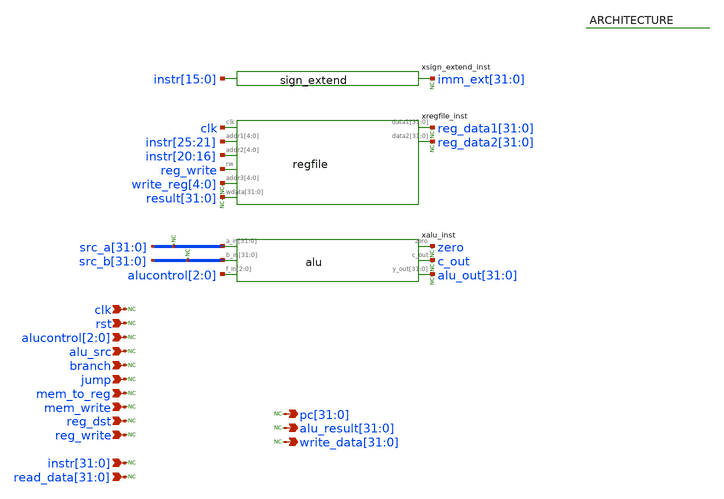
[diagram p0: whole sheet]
** sch_path: sky130A/xschem_libs/mips_cpu/datapath/schematic/datapath.sch
* Licensed under the Apache License, Version 2.0 (the "License");
* you may not use this file except in compliance with the License.
* You may obtain a copy of the License at
* https://www.apache.org/licenses/LICENSE-2.0
* Unless required by applicable law or agreed to in writing, software
* distributed under the License is distributed on an "AS IS" BASIS,
* WITHOUT WARRANTIES OR CONDITIONS OF ANY KIND, either express or implied.
* See the License for the specific language governing permissions and
* limitations under the License.
**.subckt datapath clk rst alucontrol[2],alucontrol[1],alucontrol[0] alu_src branch jump mem_to_reg
*+ reg_dst reg_write
*+ instr[31],instr[30],instr[29],instr[28],instr[27],instr[26],instr[25],instr[24],instr[23],instr[22],instr[21],instr[20],instr[19],instr[18],instr[17],instr[16],instr[15],instr[14],instr[13],instr[12],instr[11],instr[10],instr[9],instr[8],instr[7],instr[6],instr[5],instr[4],instr[3],instr[2],instr[1],instr[0]
*+ pc[31],pc[30],pc[29],pc[28],pc[27],pc[26],pc[25],pc[24],pc[23],pc[22],pc[21],pc[20],pc[19],pc[18],pc[17],pc[16],pc[15],pc[14],pc[13],pc[12],pc[11],pc[10],pc[9],pc[8],pc[7],pc[6],pc[5],pc[4],pc[3],pc[2],pc[1],pc[0]
*+ read_data[31],read_data[30],read_data[29],read_data[28],read_data[27],read_data[26],read_data[25],read_data[24],read_data[23],read_data[22],read_data[21],read_data[20],read_data[19],read_data[18],read_data[17],read_data[16],read_data[15],read_data[14],read_data[13],read_data[12],read_data[11],read_data[10],read_data[9],read_data[8],read_data[7],read_data[6],read_data[5],read_data[4],read_data[3],read_data[2],read_data[1],read_data[0]
*+ alu_result[31],alu_result[30],alu_result[29],alu_result[28],alu_result[27],alu_result[26],alu_result[25],alu_result[24],alu_result[23],alu_result[22],alu_result[21],alu_result[20],alu_result[19],alu_result[18],alu_result[17],alu_result[16],alu_result[15],alu_result[14],alu_result[13],alu_result[12],alu_result[11],alu_result[10],alu_result[9],alu_result[8],alu_result[7],alu_result[6],alu_result[5],alu_result[4],alu_result[3],alu_result[2],alu_result[1],alu_result[0]
*+ write_data[31],write_data[30],write_data[29],write_data[28],write_data[27],write_data[26],write_data[25],write_data[24],write_data[23],write_data[22],write_data[21],write_data[20],write_data[19],write_data[18],write_data[17],write_data[16],write_data[15],write_data[14],write_data[13],write_data[12],write_data[11],write_data[10],write_data[9],write_data[8],write_data[7],write_data[6],write_data[5],write_data[4],write_data[3],write_data[2],write_data[1],write_data[0] mem_write
*.ipin clk
*.ipin rst
*.ipin alucontrol[2],alucontrol[1],alucontrol[0]
*.ipin alu_src
*.ipin branch
*.ipin jump
*.ipin mem_to_reg
*.ipin reg_dst
*.ipin reg_write
*.ipin
*+ instr[31],instr[30],instr[29],instr[28],instr[27],instr[26],instr[25],instr[24],instr[23],instr[22],instr[21],instr[20],instr[19],instr[18],instr[17],instr[16],instr[15],instr[14],instr[13],instr[12],instr[11],instr[10],instr[9],instr[8],instr[7],instr[6],instr[5],instr[4],instr[3],instr[2],instr[1],instr[0]
*.opin
*+ pc[31],pc[30],pc[29],pc[28],pc[27],pc[26],pc[25],pc[24],pc[23],pc[22],pc[21],pc[20],pc[19],pc[18],pc[17],pc[16],pc[15],pc[14],pc[13],pc[12],pc[11],pc[10],pc[9],pc[8],pc[7],pc[6],pc[5],pc[4],pc[3],pc[2],pc[1],pc[0]
*.ipin
*+ read_data[31],read_data[30],read_data[29],read_data[28],read_data[27],read_data[26],read_data[25],read_data[24],read_data[23],read_data[22],read_data[21],read_data[20],read_data[19],read_data[18],read_data[17],read_data[16],read_data[15],read_data[14],read_data[13],read_data[12],read_data[11],read_data[10],read_data[9],read_data[8],read_data[7],read_data[6],read_data[5],read_data[4],read_data[3],read_data[2],read_data[1],read_data[0]
*.opin
*+ alu_result[31],alu_result[30],alu_result[29],alu_result[28],alu_result[27],alu_result[26],alu_result[25],alu_result[24],alu_result[23],alu_result[22],alu_result[21],alu_result[20],alu_result[19],alu_result[18],alu_result[17],alu_result[16],alu_result[15],alu_result[14],alu_result[13],alu_result[12],alu_result[11],alu_result[10],alu_result[9],alu_result[8],alu_result[7],alu_result[6],alu_result[5],alu_result[4],alu_result[3],alu_result[2],alu_result[1],alu_result[0]
*.opin
*+ write_data[31],write_data[30],write_data[29],write_data[28],write_data[27],write_data[26],write_data[25],write_data[24],write_data[23],write_data[22],write_data[21],write_data[20],write_data[19],write_data[18],write_data[17],write_data[16],write_data[15],write_data[14],write_data[13],write_data[12],write_data[11],write_data[10],write_data[9],write_data[8],write_data[7],write_data[6],write_data[5],write_data[4],write_data[3],write_data[2],write_data[1],write_data[0]
*.ipin mem_write
xregfile_inst clk instr[25] instr[24] instr[23] instr[22] instr[21] instr[20] instr[19] instr[18]
+ instr[17] instr[16] reg_data1[31] reg_data1[30] reg_data1[29] reg_data1[28] reg_data1[27] reg_data1[26]
+ reg_data1[25] reg_data1[24] reg_data1[23] reg_data1[22] reg_data1[21] reg_data1[20] reg_data1[19] reg_data1[18]
+ reg_data1[17] reg_data1[16] reg_data1[15] reg_data1[14] reg_data1[13] reg_data1[12] reg_data1[11] reg_data1[10]
+ reg_data1[9] reg_data1[8] reg_data1[7] reg_data1[6] reg_data1[5] reg_data1[4] reg_data1[3] reg_data1[2]
+ reg_data1[1] reg_data1[0] reg_write reg_data2[31] reg_data2[30] reg_data2[29] reg_data2[28] reg_data2[27]
+ reg_data2[26] reg_data2[25] reg_data2[24] reg_data2[23] reg_data2[22] reg_data2[21] reg_data2[20] reg_data2[19]
+ reg_data2[18] reg_data2[17] reg_data2[16] reg_data2[15] reg_data2[14] reg_data2[13] reg_data2[12] reg_data2[11]
+ reg_data2[10] reg_data2[9] reg_data2[8] reg_data2[7] reg_data2[6] reg_data2[5] reg_data2[4] reg_data2[3]
+ reg_data2[2] reg_data2[1] reg_data2[0] write_reg[4] write_reg[3] write_reg[2] write_reg[1] write_reg[0]
+ result[31] result[30] result[29] result[28] result[27] result[26] result[25] result[24] result[23] result[22]
+ result[21] result[20] result[19] result[18] result[17] result[16] result[15] result[14] result[13] result[12]
+ result[11] result[10] result[9] result[8] result[7] result[6] result[5] result[4] result[3] result[2]
+ result[1] result[0] regfile
xalu_inst src_a[31] src_a[30] src_a[29] src_a[28] src_a[27] src_a[26] src_a[25] src_a[24] src_a[23]
+ src_a[22] src_a[21] src_a[20] src_a[19] src_a[18] src_a[17] src_a[16] src_a[15] src_a[14] src_a[13] src_a[12]
+ src_a[11] src_a[10] src_a[9] src_a[8] src_a[7] src_a[6] src_a[5] src_a[4] src_a[3] src_a[2] src_a[1] src_a[0]
+ zero src_b[31] src_b[30] src_b[29] src_b[28] src_b[27] src_b[26] src_b[25] src_b[24] src_b[23] src_b[22]
+ src_b[21] src_b[20] src_b[19] src_b[18] src_b[17] src_b[16] src_b[15] src_b[14] src_b[13] src_b[12] src_b[11]
+ src_b[10] src_b[9] src_b[8] src_b[7] src_b[6] src_b[5] src_b[4] src_b[3] src_b[2] src_b[1] src_b[0] c_out
+ alu_out[31] alu_out[30] alu_out[29] alu_out[28] alu_out[27] alu_out[26] alu_out[25] alu_out[24] alu_out[23]
+ alu_out[22] alu_out[21] alu_out[20] alu_out[19] alu_out[18] alu_out[17] alu_out[16] alu_out[15] alu_out[14]
+ alu_out[13] alu_out[12] alu_out[11] alu_out[10] alu_out[9] alu_out[8] alu_out[7] alu_out[6] alu_out[5]
+ alu_out[4] alu_out[3] alu_out[2] alu_out[1] alu_out[0] alucontrol[2] alucontrol[1] alucontrol[0] alu
xsign_extend_inst instr[15] instr[14] instr[13] instr[12] instr[11] instr[10] instr[9] instr[8]
+ instr[7] instr[6] instr[5] instr[4] instr[3] instr[2] instr[1] instr[0] imm_ext[31] imm_ext[30] imm_ext[29]
+ imm_ext[28] imm_ext[27] imm_ext[26] imm_ext[25] imm_ext[24] imm_ext[23] imm_ext[22] imm_ext[21] imm_ext[20]
+ imm_ext[19] imm_ext[18] imm_ext[17] imm_ext[16] imm_ext[15] imm_ext[14] imm_ext[13] imm_ext[12] imm_ext[11]
+ imm_ext[10] imm_ext[9] imm_ext[8] imm_ext[7] imm_ext[6] imm_ext[5] imm_ext[4] imm_ext[3] imm_ext[2] imm_ext[1]
+ imm_ext[0] sign_extend
* noconn clk
* noconn rst
* noconn alucontrol[2:0]
* noconn alu_src
* noconn branch
* noconn jump
* noconn mem_to_reg
* noconn mem_write
* noconn reg_dst
* noconn reg_write
* noconn instr[31:0]
* noconn read_data[31:0]
* noconn pc[31:0]
* noconn write_data[31:0]
* noconn alu_result[31:0]
* noconn alu_out[31:0]
* noconn src_a[31:0]
* noconn src_b[31:0]
* noconn imm_ext[31:0]
* noconn reg_data1[31:0]
* noconn reg_data2[31:0]
* noconn result[31:0]
* noconn c_out
* noconn zero
* noconn write_reg[4:0]
**.ends
.end
